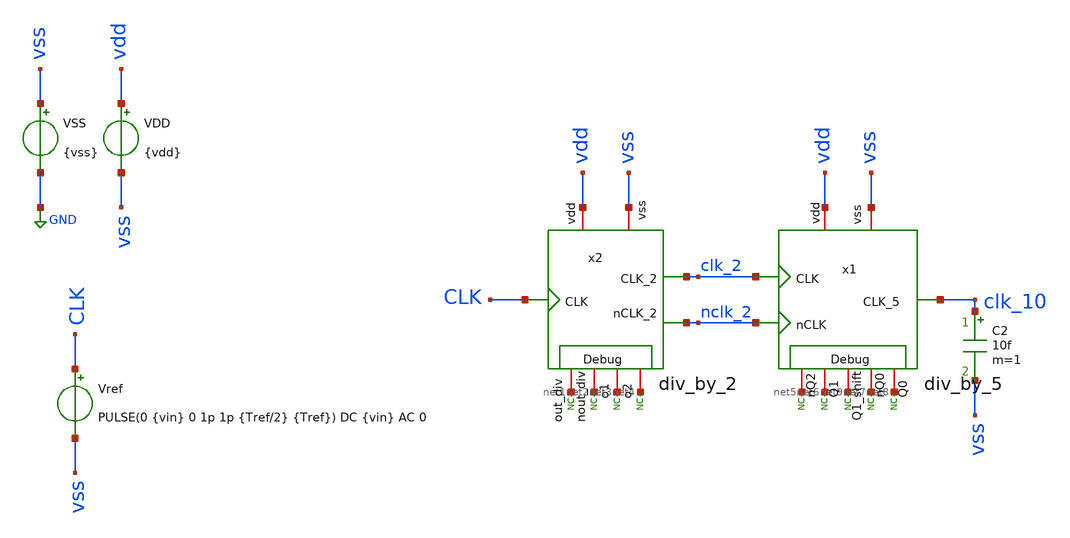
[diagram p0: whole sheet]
** sch_path: xschem/tb_div_by_5.sch
**.subckt tb_div_by_5
VSS vss GND {vss}
VDD vdd vss {vdd}
Vref CLK vss PULSE(0 {vin} 0 1p 1p {Tref/2} {Tref}) DC {vin} AC 0
C2 clk_10 vss 10f m=1
x2 nclk_2 vss CLK vdd clk_2 net1 net2 net3 net4 div_by_2
x1 vdd clk_10 clk_2 vss nclk_2 net5 net6 net7 net8 net9 div_by_5
* noconn #net5
* noconn #net6
* noconn #net9
* noconn #net7
* noconn #net8
* noconn #net1
* noconn #net2
* noconn #net3
* noconn #net4
**** begin user architecture code



* Parameters
.param kp = 1.0
.param vdd = kp*1.8
.param vss = 0.0
.param vin = vdd
.param fref = 100e6
.param Tref = 1/fref
.param C = 1f
.param iref=100u

.options TEMP = 100.0
.options RSHUNT = 1e20

* Models
.lib ~/skywater/skywater-pdk/libraries/sky130_fd_pr_ngspice/latest/models/corners/sky130.lib SS

* Data to save
.save all

.ic v(CLK) = 0.0
.ic v(x1.q2) = 0.0
.ic v(x1.q1) = 0.0
.ic v(x1.q1_shift) = 0.0
.ic v(x1.q0) = 0.0
.ic v(x1.x1.a) = 0.0
.ic v(x1.x1.D_d) = 0.0
.ic v(x1.x1.nD_d) = 0.0

* Simulation
.control
	tran 0.01ns 600ns
	*meas tran Tosc trig v(out) val=0.9 fall=5 targ v(out) val=0.9 fall=15
	*meas tran Td1  trig v(out) val=0.9 fall=5 targ v(out1) val=0.9 rise=6
	*meas tran Td2  trig v(out1) val=0.9 fall=5 targ v(out2) val=0.9 rise=6
	*meas tran Td3  trig v(out2) val=0.9 fall=5 targ v(out) val=0.9 rise=5
	*let  T = Tosc/10.0
	*let  f = 1/T
	*let Td = 1/(2*3*f)
	*print T f Td
	write tb_div_by_5_tran.raw
	plot v(clk_10) v(clk) v(clk_2) v(clk_2)+3 v(clk)+6
	plot v(x1.Q2) v(x1.Q1)+2 v(clk_Q0)+4 v(x1.Q1_shift)+6 v(clk_10)+8

.endc

.end


**** end user architecture code
**.ends
.GLOBAL GND
**** begin user architecture code
[sky130_models]
**** end user architecture code
.end
